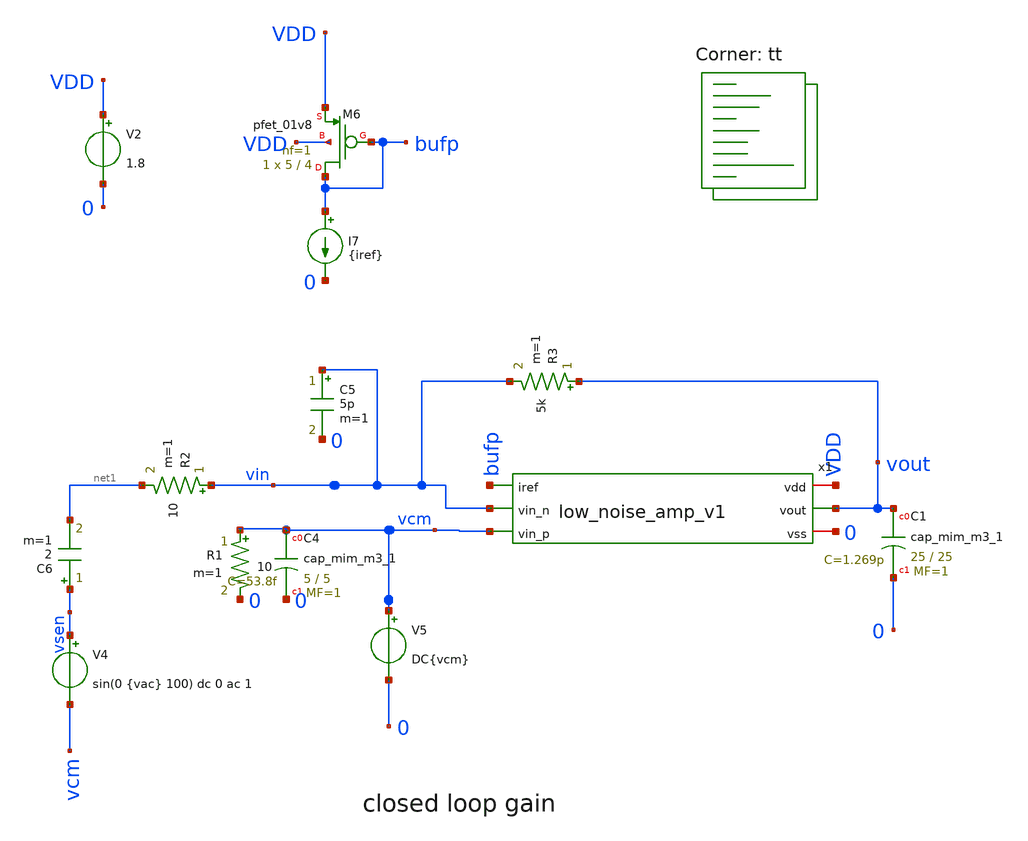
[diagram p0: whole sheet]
** sch_path: design/xschem/low_noise_amp_tb.sch
**.subckt low_noise_amp_tb
V2 VDD 0 1.8
XC1 vout 0 sky130_fd_pr__cap_mim_m3_1 W=25 L=25 MF=1 m=1
V5 vcm 0 DC{vcm}
V4 vsen vcm sin(0 {vac} 100) dc 0 ac 1
R3 vout vin 5k m=1
x1 VDD bufp vin vcm vout 0 low_noise_amp_v1
XM6 bufp bufp VDD VDD sky130_fd_pr__pfet_01v8 L=4 W=5 nf=1 ad='W * 0.29' as='W * 0.29' pd='2 * (W + 0.29)'
+ ps='2 * (W + 0.29)' nrd='0.29 / W' nrs='0.29 / W' sa=0 sb=0 sd=0 mult=1 m=1
I7 bufp 0 {iref}
XC4 vcm 0 sky130_fd_pr__cap_mim_m3_1 W=5 L=5 MF=1 m=1
R1 net2 0 10 m=1
C6 vsen net1 2 m=1
C5 vin 0 5p m=1
R2 vin net3 10 m=1
**** begin user architecture code
.lib $::SKYWATER_MODELS/sky130.lib.spice tt




* Circuit Parameters
.param iref = 500p
.param vdd  = 1.8
.param vss  = 0.0
.param vcm  = 0.8
.param vac  = 1m
.options TEMP = 65.0


* OP Parameters & Singals to save
.save all  @M.X1.XM4.msky130_fd_pr__pfet_01v8[id] @M.X1.XM4.msky130_fd_pr__pfet_01v8[vth] @M.X1.XM4.msky130_fd_pr__pfet_01v8[vgs] @M.X1.XM4.msky130_fd_pr__pfet_01v8[vds] @M.X1.XM4.msky130_fd_pr__pfet_01v8[vdsat] @M.X1.XM4.msky130_fd_pr__pfet_01v8[gm] @M.X1.XM4.msky130_fd_pr__pfet_01v8[gds]  @M.X1.XM2.msky130_fd_pr__pfet_01v8[id] @M.X1.XM2.msky130_fd_pr__pfet_01v8[vth] @M.X1.XM2.msky130_fd_pr__pfet_01v8[vgs] @M.X1.XM2.msky130_fd_pr__pfet_01v8[vds] @M.X1.XM2.msky130_fd_pr__pfet_01v8[vdsat] @M.X1.XM2.msky130_fd_pr__pfet_01v8[gm] @M.X1.XM2.msky130_fd_pr__pfet_01v8[gds]  @M.X1.XM3.msky130_fd_pr__pfet_01v8[id] @M.X1.XM3.msky130_fd_pr__pfet_01v8[vth] @M.X1.XM3.msky130_fd_pr__pfet_01v8[vgs] @M.X1.XM3.msky130_fd_pr__pfet_01v8[vds] @M.X1.XM3.msky130_fd_pr__pfet_01v8[vdsat] @M.X1.XM3.msky130_fd_pr__pfet_01v8[gm] @M.X1.XM3.msky130_fd_pr__pfet_01v8[gds]  @M.X1.XM1.msky130_fd_pr__nfet_01v8[id] @M.X1.XM1.msky130_fd_pr__nfet_01v8[vth] @M.X1.XM1.msky130_fd_pr__nfet_01v8[vgs] @M.X1.XM1.msky130_fd_pr__nfet_01v8[vds] @M.X1.XM1.msky130_fd_pr__nfet_01v8[vdsat] @M.X1.XM1.msky130_fd_pr__nfet_01v8[gm] @M.X1.XM1.msky130_fd_pr__nfet_01v8[gds]  @M.X1.XM5.msky130_fd_pr__nfet_01v8[id] @M.X1.XM5.msky130_fd_pr__nfet_01v8[vth] @M.X1.XM5.msky130_fd_pr__nfet_01v8[vgs] @M.X1.XM5.msky130_fd_pr__nfet_01v8[vds] @M.X1.XM5.msky130_fd_pr__nfet_01v8[vdsat] @M.X1.XM5.msky130_fd_pr__nfet_01v8[gm] @M.X1.XM5.msky130_fd_pr__nfet_01v8[gds]  @M.X1.XM6.msky130_fd_pr__nfet_01v8[id] @M.X1.XM6.msky130_fd_pr__nfet_01v8[vth] @M.X1.XM6.msky130_fd_pr__nfet_01v8[vgs] @M.X1.XM6.msky130_fd_pr__nfet_01v8[vds] @M.X1.XM6.msky130_fd_pr__nfet_01v8[vdsat] @M.X1.XM6.msky130_fd_pr__nfet_01v8[gm] @M.X1.XM6.msky130_fd_pr__nfet_01v8[gds]  @M.X1.XM7.msky130_fd_pr__nfet_01v8[id] @M.X1.XM7.msky130_fd_pr__nfet_01v8[vth] @M.X1.XM7.msky130_fd_pr__nfet_01v8[vgs] @M.X1.XM7.msky130_fd_pr__nfet_01v8[vds] @M.X1.XM7.msky130_fd_pr__nfet_01v8[vdsat] @M.X1.XM7.msky130_fd_pr__nfet_01v8[gm] @M.X1.XM7.msky130_fd_pr__nfet_01v8[gds]  @M.X1.XM8.msky130_fd_pr__pfet_01v8[id] @M.X1.XM8.msky130_fd_pr__pfet_01v8[vth] @M.X1.XM8.msky130_fd_pr__pfet_01v8[vgs] @M.X1.XM8.msky130_fd_pr__pfet_01v8[vds] @M.X1.XM8.msky130_fd_pr__pfet_01v8[vdsat] @M.X1.XM8.msky130_fd_pr__pfet_01v8[gm] @M.X1.XM8.msky130_fd_pr__pfet_01v8[gds]  @M.X1.XM9.msky130_fd_pr__pfet_01v8[id] @M.X1.XM9.msky130_fd_pr__pfet_01v8[vth] @M.X1.XM9.msky130_fd_pr__pfet_01v8[vgs] @M.X1.XM9.msky130_fd_pr__pfet_01v8[vds] @M.X1.XM9.msky130_fd_pr__pfet_01v8[vdsat] @M.X1.XM9.msky130_fd_pr__pfet_01v8[gm] @M.X1.XM9.msky130_fd_pr__pfet_01v8[gds]

*Simulations

.control
  ac dec 100 1k 10G
  setplot ac1
  meas ac GBW when vdb(vout)=0
  meas ac DCG find vdb(vout) at=1k
  *meas ac PM find vp(vout) when vdb(vout)=0
  *print PM*180/PI
  *meas ac GM find vdb(vout) when vp(vout)=0
  plot vdb(vout) {vp(vout)*180/PI}
  write opamp_closeloop_ac1.raw

  reset
  tran 0.1u 20m
  setplot tran1
  plot v(vsen) v(vout)
  write opamp_closeloop_tran1.raw

  reset
  noise v(vout) V4 dec 100 1k 10G 1
  setplot noise1
  plot inoise_spectrum onoise_spectrum
  *print inoise_spectrum
  *print onoise_spectrum
  setplot noise2
  *plot inoise_total onoise_total
  print inoise_total
  print onoise_total
  write opamp_closeloop_noise.raw

  reset
  op
  setplot op1
  print vout
  write opamp_closeloop_op1_today.raw

.endc

.end


**** end user architecture code
**.ends

* expanding   symbol:  low_noise_amp_v1.sym # of pins=6
** sym_path: design/xschem/low_noise_amp_v1.sym
** sch_path: design/xschem/low_noise_amp_v1.sch
.subckt low_noise_amp_v1 vdd iref vin_n vin_p vout vss
*.ipin iref
*.ipin vin_p
*.ipin vin_n
*.iopin vdd
*.iopin vss
*.opin vout
XM1 lab0 lab0 vss vss sky130_fd_pr__nfet_01v8 L=8 W=2 nf=1 ad='W * 0.29' as='W * 0.29' pd='2 * (W + 0.29)'
+ ps='2 * (W + 0.29)' nrd='0.29 / W' nrs='0.29 / W' sa=0 sb=0 sd=0 mult=1 m=1
XM2 lab0 vin_p vpn vdd sky130_fd_pr__pfet_01v8 L=2 W=4 nf=1 ad='W * 0.29' as='W * 0.29' pd='2 * (W + 0.29)'
+ ps='2 * (W + 0.29)' nrd='0.29 / W' nrs='0.29 / W' sa=0 sb=0 sd=0 mult=1 m=1
XM3 lab2 vin_n vpn vdd sky130_fd_pr__pfet_01v8 L=2 W=4 nf=1 ad='W * 0.29' as='W * 0.29' pd='2 * (W + 0.29)'
+ ps='2 * (W + 0.29)' nrd='0.29 / W' nrs='0.29 / W' sa=0 sb=0 sd=0 mult=1 m=1
XM4 vpn iref vdd vdd sky130_fd_pr__pfet_01v8 L=4 W=5 nf=1 ad='W * 0.29' as='W * 0.29' pd='2 * (W + 0.29)'
+ ps='2 * (W + 0.29)' nrd='0.29 / W' nrs='0.29 / W' sa=0 sb=0 sd=0 mult=1 m=1
XM5 lab2 lab2 vss vss sky130_fd_pr__nfet_01v8 L=8 W=2 nf=1 ad='W * 0.29' as='W * 0.29' pd='2 * (W + 0.29)'
+ ps='2 * (W + 0.29)' nrd='0.29 / W' nrs='0.29 / W' sa=0 sb=0 sd=0 mult=1 m=1
XM6 lab1 lab0 vss vss sky130_fd_pr__nfet_01v8 L=4 W=0.8 nf=1 ad='W * 0.29' as='W * 0.29' pd='2 * (W + 0.29)'
+ ps='2 * (W + 0.29)' nrd='0.29 / W' nrs='0.29 / W' sa=0 sb=0 sd=0 mult=1 m=1
XM7 vout lab2 vss vss sky130_fd_pr__nfet_01v8 L=4 W=0.8 nf=1 ad='W * 0.29' as='W * 0.29' pd='2 * (W + 0.29)'
+ ps='2 * (W + 0.29)' nrd='0.29 / W' nrs='0.29 / W' sa=0 sb=0 sd=0 mult=1 m=1
XM8 lab1 lab1 vdd vdd sky130_fd_pr__pfet_01v8 L=4 W=1.4 nf=1 ad='W * 0.29' as='W * 0.29' pd='2 * (W + 0.29)'
+ ps='2 * (W + 0.29)' nrd='0.29 / W' nrs='0.29 / W' sa=0 sb=0 sd=0 mult=1 m=1
XM9 vout lab1 vdd vdd sky130_fd_pr__pfet_01v8 L=4 W=1.4 nf=1 ad='W * 0.29' as='W * 0.29' pd='2 * (W + 0.29)'
+ ps='2 * (W + 0.29)' nrd='0.29 / W' nrs='0.29 / W' sa=0 sb=0 sd=0 mult=1 m=1
.ends

.end
